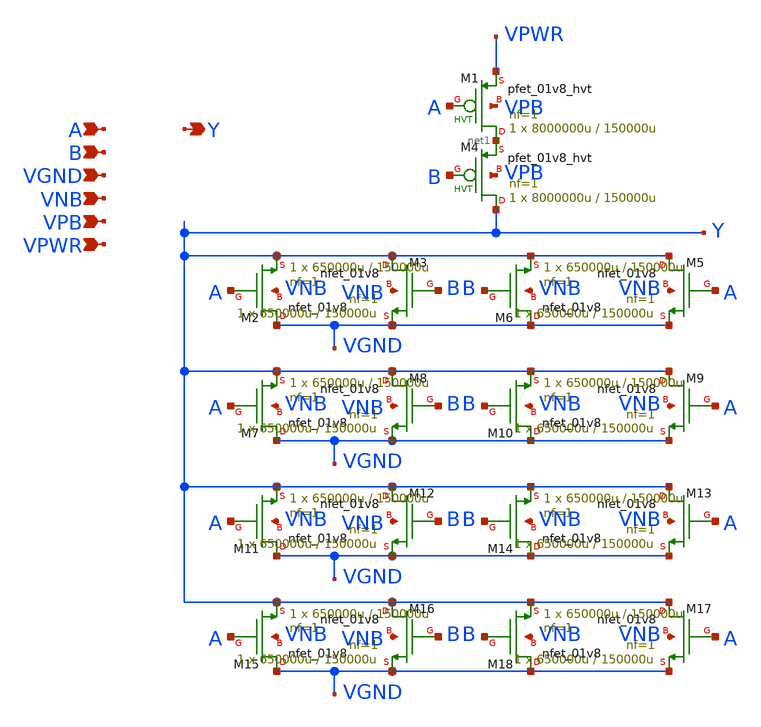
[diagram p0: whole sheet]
** sch_path: schematics/nor2/sky130_fd_sc_hd__nor2_8.sch
**.subckt sky130_fd_sc_hd__nor2_8 A Y B VGND VNB VPB VPWR
*.ipin A
*.opin Y
*.ipin B
*.ipin VGND
*.ipin VNB
*.ipin VPB
*.ipin VPWR
XM2 VGND A Y VNB sky130_fd_pr__nfet_01v8 L=150000u W=650000u nf=1 ad='int((1 + 1)/2) * 650000u / 1 * 0.29'
+ as='int((1 + 2)/2) * 650000u / 1 * 0.29' pd='2*int((1 + 1)/2) * (650000u / 1 + 0.29)' ps='2*int((1 + 2)/2) * (650000u / 1 + 0.29)'
+ nrd='0.29 / 650000u ' nrs='0.29 / 650000u ' sa=0 sb=0 sd=0 mult=1 m=1
XM3 Y B VGND VNB sky130_fd_pr__nfet_01v8 L=150000u W=650000u nf=1 ad='int((1 + 1)/2) * 650000u / 1 * 0.29'
+ as='int((1 + 2)/2) * 650000u / 1 * 0.29' pd='2*int((1 + 1)/2) * (650000u / 1 + 0.29)' ps='2*int((1 + 2)/2) * (650000u / 1 + 0.29)'
+ nrd='0.29 / 650000u ' nrs='0.29 / 650000u ' sa=0 sb=0 sd=0 mult=1 m=1
XM5 Y A VGND VNB sky130_fd_pr__nfet_01v8 L=150000u W=650000u nf=1 ad='int((1 + 1)/2) * 650000u / 1 * 0.29'
+ as='int((1 + 2)/2) * 650000u / 1 * 0.29' pd='2*int((1 + 1)/2) * (650000u / 1 + 0.29)' ps='2*int((1 + 2)/2) * (650000u / 1 + 0.29)'
+ nrd='0.29 / 650000u ' nrs='0.29 / 650000u ' sa=0 sb=0 sd=0 mult=1 m=1
XM6 VGND B Y VNB sky130_fd_pr__nfet_01v8 L=150000u W=650000u nf=1 ad='int((1 + 1)/2) * 650000u / 1 * 0.29'
+ as='int((1 + 2)/2) * 650000u / 1 * 0.29' pd='2*int((1 + 1)/2) * (650000u / 1 + 0.29)' ps='2*int((1 + 2)/2) * (650000u / 1 + 0.29)'
+ nrd='0.29 / 650000u ' nrs='0.29 / 650000u ' sa=0 sb=0 sd=0 mult=1 m=1
XM1 net1 A VPWR VPB sky130_fd_pr__pfet_01v8_hvt L=150000u W=8000000u nf=1 ad='int((1 + 1)/2) * 8000000u / 1 * 0.29'
+ as='int((1 + 2)/2) * 8000000u / 1 * 0.29' pd='2*int((1 + 1)/2) * (8000000u / 1 + 0.29)' ps='2*int((1 + 2)/2) * (8000000u / 1 + 0.29)'
+ nrd='0.29 / 8000000u ' nrs='0.29 / 8000000u ' sa=0 sb=0 sd=0 mult=1 m=1
XM4 Y B net1 VPB sky130_fd_pr__pfet_01v8_hvt L=150000u W=8000000u nf=1 ad='int((1 + 1)/2) * 8000000u / 1 * 0.29'
+ as='int((1 + 2)/2) * 8000000u / 1 * 0.29' pd='2*int((1 + 1)/2) * (8000000u / 1 + 0.29)' ps='2*int((1 + 2)/2) * (8000000u / 1 + 0.29)'
+ nrd='0.29 / 8000000u ' nrs='0.29 / 8000000u ' sa=0 sb=0 sd=0 mult=1 m=1
XM7 VGND A Y VNB sky130_fd_pr__nfet_01v8 L=150000u W=650000u nf=1 ad='int((1 + 1)/2) * 650000u / 1 * 0.29'
+ as='int((1 + 2)/2) * 650000u / 1 * 0.29' pd='2*int((1 + 1)/2) * (650000u / 1 + 0.29)' ps='2*int((1 + 2)/2) * (650000u / 1 + 0.29)'
+ nrd='0.29 / 650000u ' nrs='0.29 / 650000u ' sa=0 sb=0 sd=0 mult=1 m=1
XM8 Y B VGND VNB sky130_fd_pr__nfet_01v8 L=150000u W=650000u nf=1 ad='int((1 + 1)/2) * 650000u / 1 * 0.29'
+ as='int((1 + 2)/2) * 650000u / 1 * 0.29' pd='2*int((1 + 1)/2) * (650000u / 1 + 0.29)' ps='2*int((1 + 2)/2) * (650000u / 1 + 0.29)'
+ nrd='0.29 / 650000u ' nrs='0.29 / 650000u ' sa=0 sb=0 sd=0 mult=1 m=1
XM9 Y A VGND VNB sky130_fd_pr__nfet_01v8 L=150000u W=650000u nf=1 ad='int((1 + 1)/2) * 650000u / 1 * 0.29'
+ as='int((1 + 2)/2) * 650000u / 1 * 0.29' pd='2*int((1 + 1)/2) * (650000u / 1 + 0.29)' ps='2*int((1 + 2)/2) * (650000u / 1 + 0.29)'
+ nrd='0.29 / 650000u ' nrs='0.29 / 650000u ' sa=0 sb=0 sd=0 mult=1 m=1
XM10 VGND B Y VNB sky130_fd_pr__nfet_01v8 L=150000u W=650000u nf=1 ad='int((1 + 1)/2) * 650000u / 1 * 0.29'
+ as='int((1 + 2)/2) * 650000u / 1 * 0.29' pd='2*int((1 + 1)/2) * (650000u / 1 + 0.29)' ps='2*int((1 + 2)/2) * (650000u / 1 + 0.29)'
+ nrd='0.29 / 650000u ' nrs='0.29 / 650000u ' sa=0 sb=0 sd=0 mult=1 m=1
XM11 VGND A Y VNB sky130_fd_pr__nfet_01v8 L=150000u W=650000u nf=1 ad='int((1 + 1)/2) * 650000u / 1 * 0.29'
+ as='int((1 + 2)/2) * 650000u / 1 * 0.29' pd='2*int((1 + 1)/2) * (650000u / 1 + 0.29)' ps='2*int((1 + 2)/2) * (650000u / 1 + 0.29)'
+ nrd='0.29 / 650000u ' nrs='0.29 / 650000u ' sa=0 sb=0 sd=0 mult=1 m=1
XM12 Y B VGND VNB sky130_fd_pr__nfet_01v8 L=150000u W=650000u nf=1 ad='int((1 + 1)/2) * 650000u / 1 * 0.29'
+ as='int((1 + 2)/2) * 650000u / 1 * 0.29' pd='2*int((1 + 1)/2) * (650000u / 1 + 0.29)' ps='2*int((1 + 2)/2) * (650000u / 1 + 0.29)'
+ nrd='0.29 / 650000u ' nrs='0.29 / 650000u ' sa=0 sb=0 sd=0 mult=1 m=1
XM13 Y A VGND VNB sky130_fd_pr__nfet_01v8 L=150000u W=650000u nf=1 ad='int((1 + 1)/2) * 650000u / 1 * 0.29'
+ as='int((1 + 2)/2) * 650000u / 1 * 0.29' pd='2*int((1 + 1)/2) * (650000u / 1 + 0.29)' ps='2*int((1 + 2)/2) * (650000u / 1 + 0.29)'
+ nrd='0.29 / 650000u ' nrs='0.29 / 650000u ' sa=0 sb=0 sd=0 mult=1 m=1
XM14 VGND B Y VNB sky130_fd_pr__nfet_01v8 L=150000u W=650000u nf=1 ad='int((1 + 1)/2) * 650000u / 1 * 0.29'
+ as='int((1 + 2)/2) * 650000u / 1 * 0.29' pd='2*int((1 + 1)/2) * (650000u / 1 + 0.29)' ps='2*int((1 + 2)/2) * (650000u / 1 + 0.29)'
+ nrd='0.29 / 650000u ' nrs='0.29 / 650000u ' sa=0 sb=0 sd=0 mult=1 m=1
XM15 VGND A Y VNB sky130_fd_pr__nfet_01v8 L=150000u W=650000u nf=1 ad='int((1 + 1)/2) * 650000u / 1 * 0.29'
+ as='int((1 + 2)/2) * 650000u / 1 * 0.29' pd='2*int((1 + 1)/2) * (650000u / 1 + 0.29)' ps='2*int((1 + 2)/2) * (650000u / 1 + 0.29)'
+ nrd='0.29 / 650000u ' nrs='0.29 / 650000u ' sa=0 sb=0 sd=0 mult=1 m=1
XM16 Y B VGND VNB sky130_fd_pr__nfet_01v8 L=150000u W=650000u nf=1 ad='int((1 + 1)/2) * 650000u / 1 * 0.29'
+ as='int((1 + 2)/2) * 650000u / 1 * 0.29' pd='2*int((1 + 1)/2) * (650000u / 1 + 0.29)' ps='2*int((1 + 2)/2) * (650000u / 1 + 0.29)'
+ nrd='0.29 / 650000u ' nrs='0.29 / 650000u ' sa=0 sb=0 sd=0 mult=1 m=1
XM17 Y A VGND VNB sky130_fd_pr__nfet_01v8 L=150000u W=650000u nf=1 ad='int((1 + 1)/2) * 650000u / 1 * 0.29'
+ as='int((1 + 2)/2) * 650000u / 1 * 0.29' pd='2*int((1 + 1)/2) * (650000u / 1 + 0.29)' ps='2*int((1 + 2)/2) * (650000u / 1 + 0.29)'
+ nrd='0.29 / 650000u ' nrs='0.29 / 650000u ' sa=0 sb=0 sd=0 mult=1 m=1
XM18 VGND B Y VNB sky130_fd_pr__nfet_01v8 L=150000u W=650000u nf=1 ad='int((1 + 1)/2) * 650000u / 1 * 0.29'
+ as='int((1 + 2)/2) * 650000u / 1 * 0.29' pd='2*int((1 + 1)/2) * (650000u / 1 + 0.29)' ps='2*int((1 + 2)/2) * (650000u / 1 + 0.29)'
+ nrd='0.29 / 650000u ' nrs='0.29 / 650000u ' sa=0 sb=0 sd=0 mult=1 m=1
**.ends
.end
